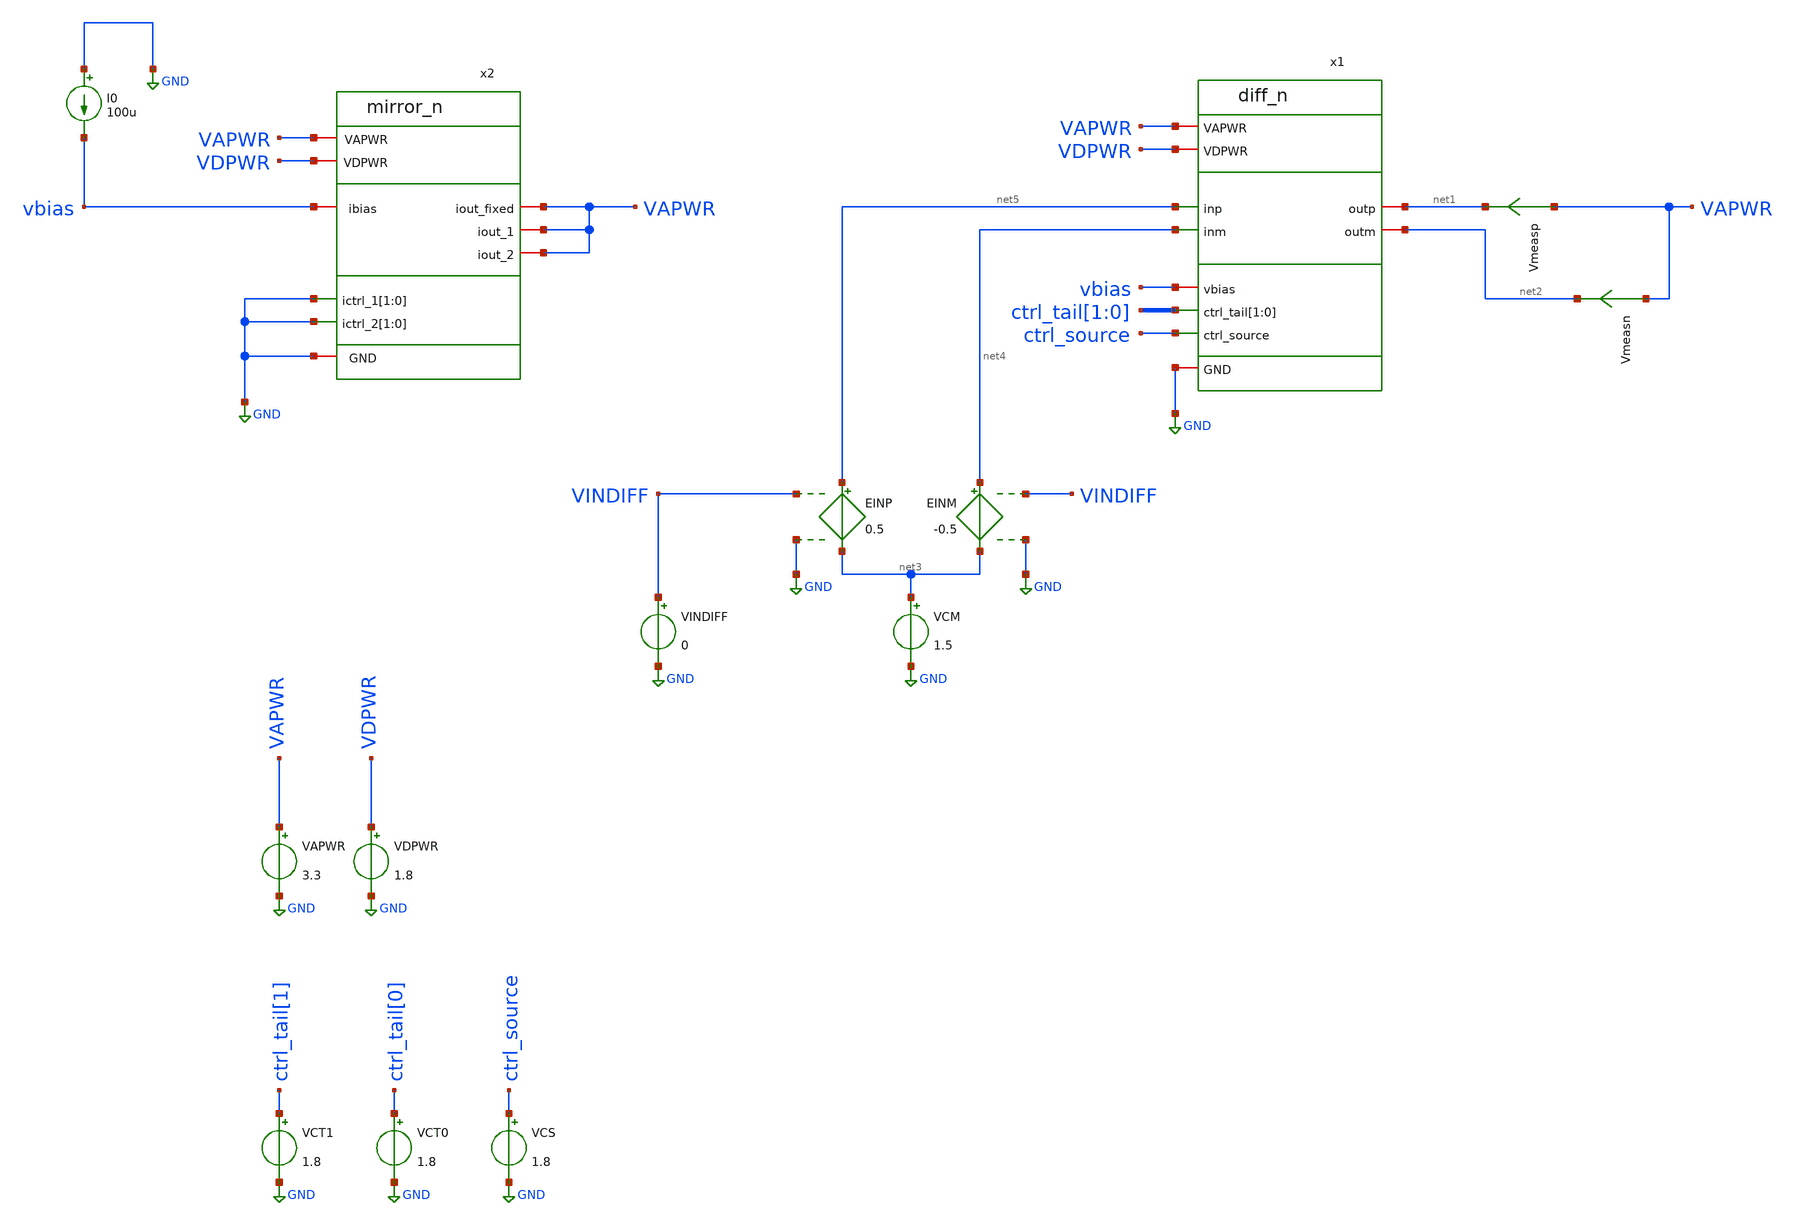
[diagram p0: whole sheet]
** sch_path: xschem/tb_diff_n.sch
**.subckt tb_diff_n
x1 VAPWR VDPWR net1 net2 net5 net4 ctrl_tail[1] ctrl_tail[0] ctrl_source vbias GND diff_n
VAPWR VAPWR GND 3.3
VDPWR VDPWR GND 1.8
x2 VAPWR VDPWR vbias VAPWR VAPWR VAPWR GND GND GND GND GND mirror_n
I0 GND vbias 100u
Vmeasp VAPWR net1 0
.save i(vmeasp)
Vmeasn VAPWR net2 0
.save i(vmeasn)
VCM net3 GND 1.5
VCT1 ctrl_tail[1] GND 1.8
VCT0 ctrl_tail[0] GND 1.8
VCS ctrl_source GND 1.8
EINP net5 net3 VINDIFF GND 0.5
EINM net4 net3 VINDIFF GND -0.5
VINDIFF VINDIFF GND 0
**** begin user architecture code
.lib $::SKYWATER_MODELS/sky130.lib.spice tt


*****************************************
* Vin DC Sweep Test
*****************************************
* this test sweeps the differential input voltage
* and plots the differential output current (and gm)
* for various magnitudes of tail current
*****************************************
.control
   save all
   set temp = 27
   set wr_singlescale
   set wr_vecnames
   alter VCM 1
   alter VCT1 0
   alter VCT0 0
   alter VCS 0
   repeat 2
      repeat 2
         dc VINDIFF -1 1 0.01
         alter VCT0 1.8
      end
      alter VCT1 1.8
      alter VCT0 0
   end
   plot (dc1.i(Vmeasp)-dc1.i(Vmeasn)) (dc2.i(Vmeasp)-dc2.i(Vmeasn)) (dc3.i(Vmeasp)-dc3.i(Vmeasn))
+ (dc4.i(Vmeasp)-dc4.i(Vmeasn))
   plot deriv(dc1.i(Vmeasp)-dc1.i(Vmeasn)) deriv(dc2.i(Vmeasp)-dc2.i(Vmeasn))
+ deriv(dc3.i(Vmeasp)-dc3.i(Vmeasn)) deriv(dc4.i(Vmeasp)-dc4.i(Vmeasn))
.endc


**** end user architecture code
**.ends
.GLOBAL GND
.end
